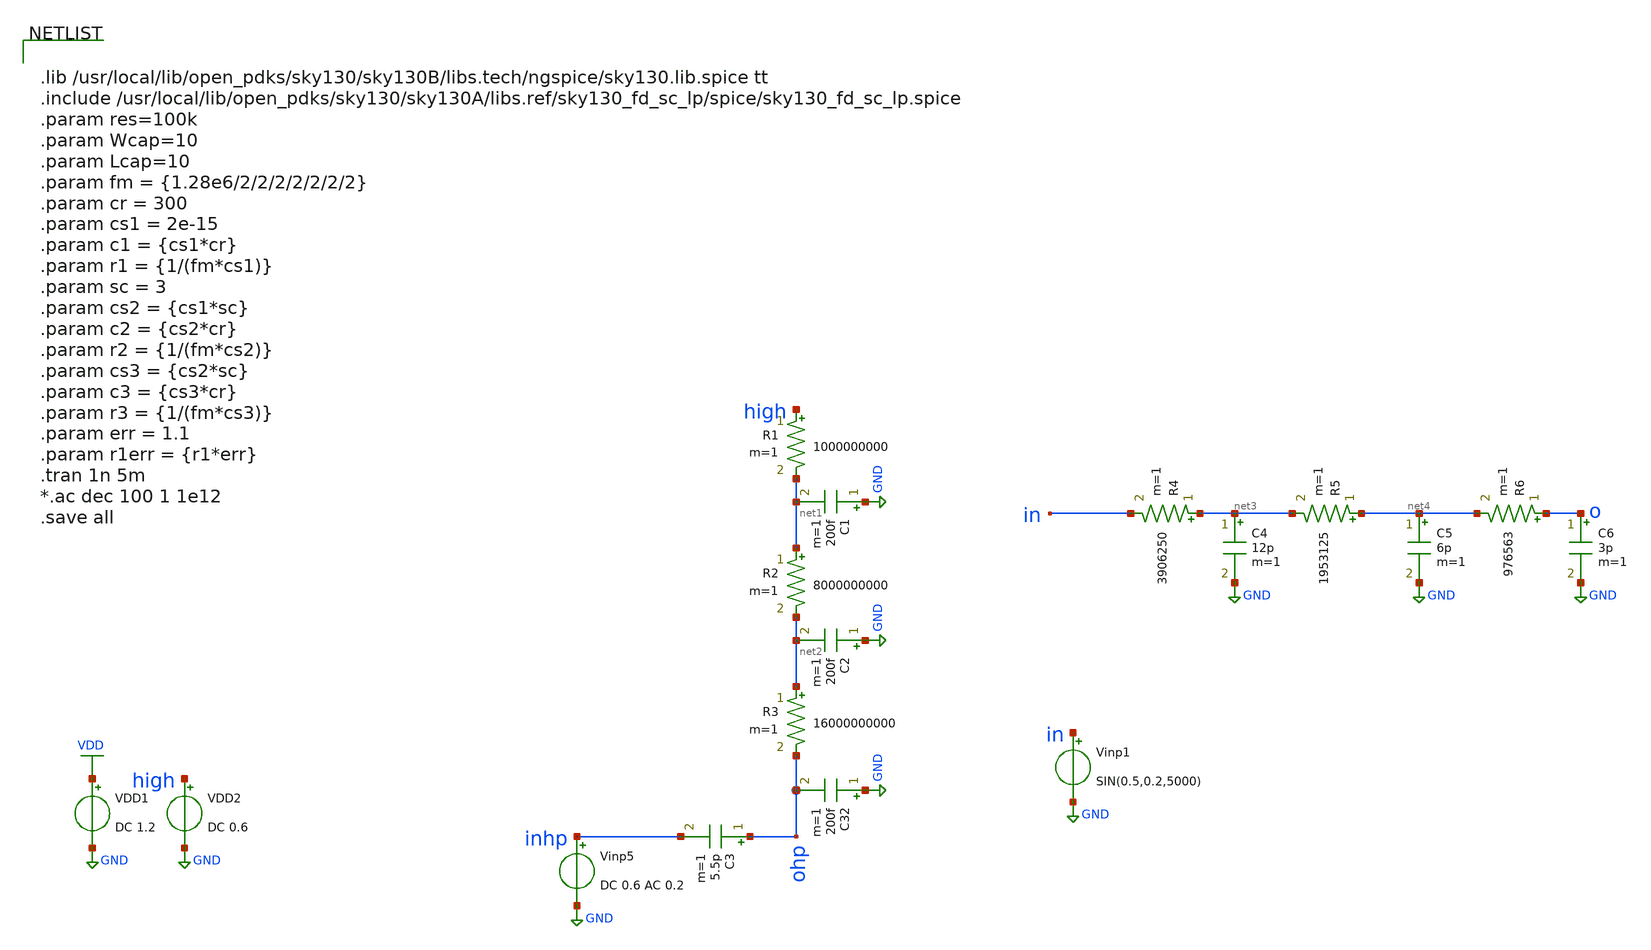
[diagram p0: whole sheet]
** sch_path: xschem/tryandtest/RCcharacterization.sch
**.subckt RCcharacterization
VDD1 VDD GND DC 1.2
C32 GND ohp 200f m=1
Vinp5 inhp GND DC 0.6 AC 0.2
R1 high net1 1000000000 m=1
R2 net1 net2 8000000000 m=1
R3 net2 ohp 16000000000 m=1
C1 GND net1 200f m=1
C2 GND net2 200f m=1
VDD2 high GND DC 0.6
C3 ohp inhp 5.5p m=1
R4 net3 in 3906250 m=1
R5 net4 net3 1953125 m=1
R6 o net4 976563 m=1
C4 net3 GND 12p m=1
C5 net4 GND 6p m=1
C6 o GND 3p m=1
Vinp1 in GND SIN(0.5,0.2,5000)
**** begin user architecture code


.lib /usr/local/lib/open_pdks/sky130/sky130B/libs.tech/ngspice/sky130.lib.spice tt
.include /usr/local/lib/open_pdks/sky130/sky130A/libs.ref/sky130_fd_sc_lp/spice/sky130_fd_sc_lp.spice
.param res=100k
.param Wcap=10
.param Lcap=10
.param fm = {1.28e6/2/2/2/2/2/2/2}
.param cr = 300
.param cs1 = 2e-15
.param c1 = {cs1*cr}
.param r1 = {1/(fm*cs1)}
.param sc = 3
.param cs2 = {cs1*sc}
.param c2 = {cs2*cr}
.param r2 = {1/(fm*cs2)}
.param cs3 = {cs2*sc}
.param c3 = {cs3*cr}
.param r3 = {1/(fm*cs3)}
.param err = 1.1
.param r1err = {r1*err}
.tran 1n 5m
*.ac dec 100 1 1e12
.save all


**** end user architecture code
**.ends
.GLOBAL GND
.GLOBAL VDD
.end
